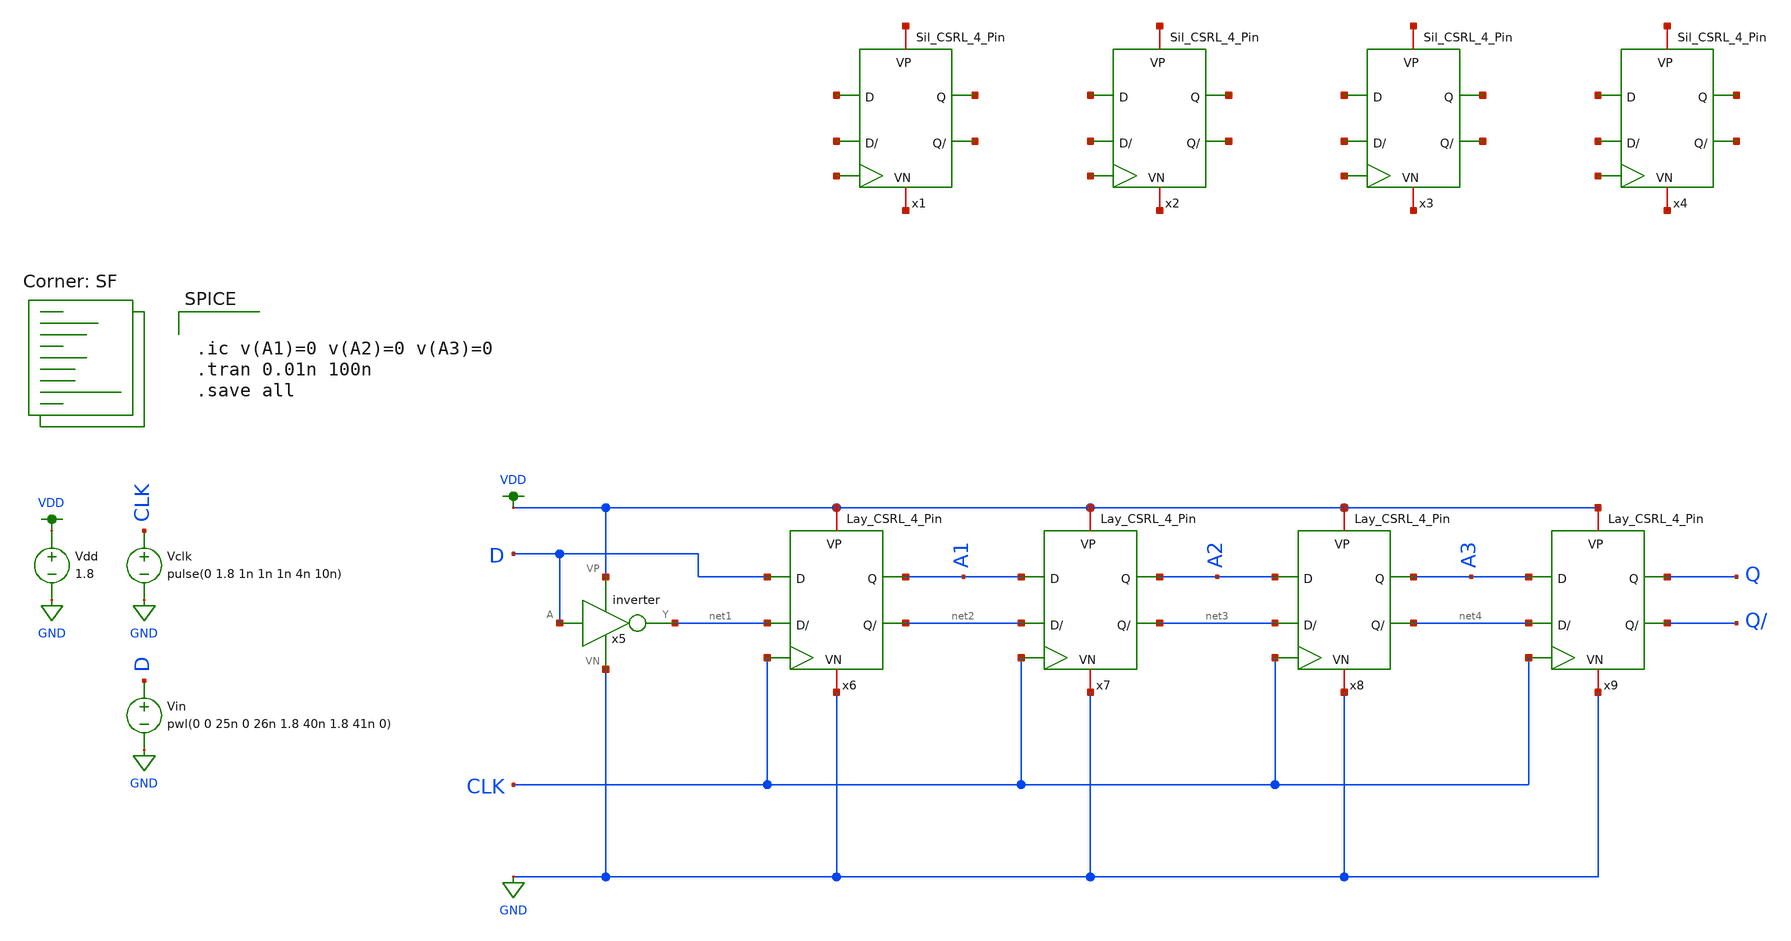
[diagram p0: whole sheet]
** sch_path: MADVLSI_MP2/Shift_Reg_V1.sch
**.subckt Shift_Reg_V1
x5 VDD D net1 GND inverter
Vdd VDD GND 1.8
Vclk CLK GND pulse(0 1.8 1n 1n 1n 4n 10n)
Vin D GND pwl(0 0 25n 0 26n 1.8 40n 1.8 41n 0)
x1 net5 net6 net7 net8 net9 net10 net11 Sil_CSRL_4_Pin
x2 net12 net13 net14 net15 net16 net17 net18 Sil_CSRL_4_Pin
x3 net19 net20 net21 net22 net23 net24 net25 Sil_CSRL_4_Pin
x4 net26 net27 net28 net29 net30 net31 net32 Sil_CSRL_4_Pin
x6 net1 CLK D VDD net2 A1 GND Lay_CSRL_4_Pin
x7 net2 CLK A1 VDD net3 A2 GND Lay_CSRL_4_Pin
x8 net3 CLK A2 VDD net4 A3 GND Lay_CSRL_4_Pin
x9 net4 CLK A3 VDD Q/ Q GND Lay_CSRL_4_Pin
**** begin user architecture code


.ic v(A1)=0 v(A2)=0 v(A3)=0
.tran 0.01n 100n
.save all

.lib $::SKYWATER_MODELS/sky130.lib.spice SF
**** end user architecture code
**.ends

* expanding   symbol:  /home/allan/Documents/MADVLSI_Projects/MADVLSI_MP1/inverter.sym # of pins=4
** sym_path: MADVLSI_MP1/inverter.sym
** sch_path: MADVLSI_MP1/inverter.sch
.subckt inverter VP A Y VN
*.ipin A
*.iopin VP
*.iopin VN
*.opin Y
XM1 Y A VN VN sky130_fd_pr__nfet_01v8 L=0.15 W=1 nf=1 ad='int((nf+1)/2) * W/nf * 0.29' as='int((nf+2)/2) * W/nf * 0.29'
+ pd='2*int((nf+1)/2) * (W/nf + 0.29)' ps='2*int((nf+2)/2) * (W/nf + 0.29)' nrd='0.29 / W' nrs='0.29 / W'
+ sa=0 sb=0 sd=0 mult=1 m=1
XM2 Y A VP VP sky130_fd_pr__pfet_01v8 L=0.15 W=1 nf=1 ad='int((nf+1)/2) * W/nf * 0.29' as='int((nf+2)/2) * W/nf * 0.29'
+ pd='2*int((nf+1)/2) * (W/nf + 0.29)' ps='2*int((nf+2)/2) * (W/nf + 0.29)' nrd='0.29 / W' nrs='0.29 / W'
+ sa=0 sb=0 sd=0 mult=1 m=1
.ends


* expanding   symbol:  Sil_CSRL_4_Pin.sym # of pins=7
** sym_path: MADVLSI_MP2/Sil_CSRL_4_Pin.sym
** sch_path: MADVLSI_MP2/Sil_CSRL_4_Pin.sch
.subckt Sil_CSRL_4_Pin VP D Q QBar DBar clk VN
*.iopin VN
*.iopin VP
*.ipin D
*.ipin DBar
*.ipin clk
*.opin Q
*.opin QBar
XQ1 net1 clk D VP sky130_fd_pr__pfet_01v8 L=0.15 W=0.9 nf=1 ad='int((nf+1)/2) * W/nf * 0.29' as='int((nf+2)/2) * W/nf * 0.29'
+ pd='2*int((nf+1)/2) * (W/nf + 0.29)' ps='2*int((nf+2)/2) * (W/nf + 0.29)' nrd='0.29 / W' nrs='0.29 / W'
+ sa=0 sb=0 sd=0 mult=1 m=1
XQ3 Q clk net1 VN sky130_fd_pr__nfet_01v8 L=0.15 W=0.9 nf=1 ad='int((nf+1)/2) * W/nf * 0.29' as='int((nf+2)/2) * W/nf * 0.29'
+ pd='2*int((nf+1)/2) * (W/nf + 0.29)' ps='2*int((nf+2)/2) * (W/nf + 0.29)' nrd='0.29 / W' nrs='0.29 / W'
+ sa=0 sb=0 sd=0 mult=1 m=1
XQ2 net2 clk DBar VP sky130_fd_pr__pfet_01v8 L=0.15 W=0.9 nf=1 ad='int((nf+1)/2) * W/nf * 0.29' as='int((nf+2)/2) * W/nf * 0.29'
+ pd='2*int((nf+1)/2) * (W/nf + 0.29)' ps='2*int((nf+2)/2) * (W/nf + 0.29)' nrd='0.29 / W' nrs='0.29 / W'
+ sa=0 sb=0 sd=0 mult=1 m=1
XQ8 net2 net1 VP VP sky130_fd_pr__pfet_01v8 L=0.15 W=0.9 nf=1 ad='int((nf+1)/2) * W/nf * 0.29' as='int((nf+2)/2) * W/nf * 0.29'
+ pd='2*int((nf+1)/2) * (W/nf + 0.29)' ps='2*int((nf+2)/2) * (W/nf + 0.29)' nrd='0.29 / W' nrs='0.29 / W'
+ sa=0 sb=0 sd=0 mult=1 m=1
XQ9 VP net2 net1 VP sky130_fd_pr__pfet_01v8 L=0.15 W=0.9 nf=1 ad='int((nf+1)/2) * W/nf * 0.29' as='int((nf+2)/2) * W/nf * 0.29'
+ pd='2*int((nf+1)/2) * (W/nf + 0.29)' ps='2*int((nf+2)/2) * (W/nf + 0.29)' nrd='0.29 / W' nrs='0.29 / W'
+ sa=0 sb=0 sd=0 mult=1 m=1
XQ12 net4 QBar Q VP sky130_fd_pr__pfet_01v8 L=0.15 W=0.9 nf=1 ad='int((nf+1)/2) * W/nf * 0.29' as='int((nf+2)/2) * W/nf * 0.29'
+ pd='2*int((nf+1)/2) * (W/nf + 0.29)' ps='2*int((nf+2)/2) * (W/nf + 0.29)' nrd='0.29 / W' nrs='0.29 / W'
+ sa=0 sb=0 sd=0 mult=1 m=1
XQ10 net4 clk VP VP sky130_fd_pr__pfet_01v8 L=0.15 W=0.9 nf=1 ad='int((nf+1)/2) * W/nf * 0.29' as='int((nf+2)/2) * W/nf * 0.29'
+ pd='2*int((nf+1)/2) * (W/nf + 0.29)' ps='2*int((nf+2)/2) * (W/nf + 0.29)' nrd='0.29 / W' nrs='0.29 / W'
+ sa=0 sb=0 sd=0 mult=1 m=1
XQ11 QBar Q net4 VP sky130_fd_pr__pfet_01v8 L=0.15 W=0.9 nf=1 ad='int((nf+1)/2) * W/nf * 0.29' as='int((nf+2)/2) * W/nf * 0.29'
+ pd='2*int((nf+1)/2) * (W/nf + 0.29)' ps='2*int((nf+2)/2) * (W/nf + 0.29)' nrd='0.29 / W' nrs='0.29 / W'
+ sa=0 sb=0 sd=0 mult=1 m=1
XQ4 QBar clk net2 VN sky130_fd_pr__nfet_01v8 L=0.15 W=0.9 nf=1 ad='int((nf+1)/2) * W/nf * 0.29' as='int((nf+2)/2) * W/nf * 0.29'
+ pd='2*int((nf+1)/2) * (W/nf + 0.29)' ps='2*int((nf+2)/2) * (W/nf + 0.29)' nrd='0.29 / W' nrs='0.29 / W'
+ sa=0 sb=0 sd=0 mult=1 m=1
XQ5a net3 clk VN VN sky130_fd_pr__nfet_01v8 L=0.15 W=0.45 nf=1 ad='int((nf+1)/2) * W/nf * 0.29' as='int((nf+2)/2) * W/nf * 0.29'
+ pd='2*int((nf+1)/2) * (W/nf + 0.29)' ps='2*int((nf+2)/2) * (W/nf + 0.29)' nrd='0.29 / W' nrs='0.29 / W'
+ sa=0 sb=0 sd=0 mult=1 m=1
XQ7 net3 net2 net1 VN sky130_fd_pr__nfet_01v8 L=0.15 W=0.45 nf=1 ad='int((nf+1)/2) * W/nf * 0.29' as='int((nf+2)/2) * W/nf * 0.29'
+ pd='2*int((nf+1)/2) * (W/nf + 0.29)' ps='2*int((nf+2)/2) * (W/nf + 0.29)' nrd='0.29 / W' nrs='0.29 / W'
+ sa=0 sb=0 sd=0 mult=1 m=1
XQ6 net2 net1 net3 VN sky130_fd_pr__nfet_01v8 L=0.15 W=0.45 nf=1 ad='int((nf+1)/2) * W/nf * 0.29' as='int((nf+2)/2) * W/nf * 0.29'
+ pd='2*int((nf+1)/2) * (W/nf + 0.29)' ps='2*int((nf+2)/2) * (W/nf + 0.29)' nrd='0.29 / W' nrs='0.29 / W'
+ sa=0 sb=0 sd=0 mult=1 m=1
XQ13 QBar Q VN VN sky130_fd_pr__nfet_01v8 L=0.15 W=0.45 nf=1 ad='int((nf+1)/2) * W/nf * 0.29' as='int((nf+2)/2) * W/nf * 0.29'
+ pd='2*int((nf+1)/2) * (W/nf + 0.29)' ps='2*int((nf+2)/2) * (W/nf + 0.29)' nrd='0.29 / W' nrs='0.29 / W'
+ sa=0 sb=0 sd=0 mult=1 m=1
XQ14 VN QBar Q VN sky130_fd_pr__nfet_01v8 L=0.15 W=0.45 nf=1 ad='int((nf+1)/2) * W/nf * 0.29' as='int((nf+2)/2) * W/nf * 0.29'
+ pd='2*int((nf+1)/2) * (W/nf + 0.29)' ps='2*int((nf+2)/2) * (W/nf + 0.29)' nrd='0.29 / W' nrs='0.29 / W'
+ sa=0 sb=0 sd=0 mult=1 m=1
XQ5b VN clk net3 VN sky130_fd_pr__nfet_01v8 L=0.15 W=0.45 nf=1 ad='int((nf+1)/2) * W/nf * 0.29' as='int((nf+2)/2) * W/nf * 0.29'
+ pd='2*int((nf+1)/2) * (W/nf + 0.29)' ps='2*int((nf+2)/2) * (W/nf + 0.29)' nrd='0.29 / W' nrs='0.29 / W'
+ sa=0 sb=0 sd=0 mult=1 m=1
XQ10b VP clk net4 VP sky130_fd_pr__pfet_01v8 L=0.15 W=0.9 nf=1 ad='int((nf+1)/2) * W/nf * 0.29' as='int((nf+2)/2) * W/nf * 0.29'
+ pd='2*int((nf+1)/2) * (W/nf + 0.29)' ps='2*int((nf+2)/2) * (W/nf + 0.29)' nrd='0.29 / W' nrs='0.29 / W'
+ sa=0 sb=0 sd=0 mult=1 m=1
.ends


* expanding   symbol:  /home/allan/Documents/MADVLSI_Projects/MADVLSI_MP2/Lay_CSRL_4_Pin.sym # of
*+ pins=7
** sym_path: MADVLSI_MP2/Lay_CSRL_4_Pin.sym
** sch_path: MADVLSI_MP2/Lay_CSRL_4_Pin.sch
.subckt Lay_CSRL_4_Pin D/ CLQ D VP Q/ Q VN
*.ipin D/
*.ipin D
*.ipin CLQ
*.iopin VP
*.iopin VN
*.opin Q/
*.opin Q
XQ2 net3 CLQ D/ VDD sky130_fd_pr__pfet_01v8 L=0.15 W=0.9 nf=1 ad='int((nf+1)/2) * W/nf * 0.29' as='int((nf+2)/2) * W/nf * 0.29'
+ pd='2*int((nf+1)/2) * (W/nf + 0.29)' ps='2*int((nf+2)/2) * (W/nf + 0.29)' nrd='0.29 / W' nrs='0.29 / W'
+ sa=0 sb=0 sd=0 mult=1 m=1
XQ8 VP net1 net3 VDD sky130_fd_pr__pfet_01v8 L=0.15 W=0.9 nf=1 ad='int((nf+1)/2) * W/nf * 0.29' as='int((nf+2)/2) * W/nf * 0.29'
+ pd='2*int((nf+1)/2) * (W/nf + 0.29)' ps='2*int((nf+2)/2) * (W/nf + 0.29)' nrd='0.29 / W' nrs='0.29 / W'
+ sa=0 sb=0 sd=0 mult=1 m=1
XQ10b net2 CLQ VP VDD sky130_fd_pr__pfet_01v8 L=0.15 W=0.9 nf=1 ad='int((nf+1)/2) * W/nf * 0.29' as='int((nf+2)/2) * W/nf * 0.29'
+ pd='2*int((nf+1)/2) * (W/nf + 0.29)' ps='2*int((nf+2)/2) * (W/nf + 0.29)' nrd='0.29 / W' nrs='0.29 / W'
+ sa=0 sb=0 sd=0 mult=1 m=1
XQ11 Q/ Q net2 VDD sky130_fd_pr__pfet_01v8 L=0.15 W=0.9 nf=1 ad='int((nf+1)/2) * W/nf * 0.29' as='int((nf+2)/2) * W/nf * 0.29'
+ pd='2*int((nf+1)/2) * (W/nf + 0.29)' ps='2*int((nf+2)/2) * (W/nf + 0.29)' nrd='0.29 / W' nrs='0.29 / W'
+ sa=0 sb=0 sd=0 mult=1 m=1
XQ1 net1 CLQ D VDD sky130_fd_pr__pfet_01v8 L=0.15 W=0.9 nf=1 ad='int((nf+1)/2) * W/nf * 0.29' as='int((nf+2)/2) * W/nf * 0.29'
+ pd='2*int((nf+1)/2) * (W/nf + 0.29)' ps='2*int((nf+2)/2) * (W/nf + 0.29)' nrd='0.29 / W' nrs='0.29 / W'
+ sa=0 sb=0 sd=0 mult=1 m=1
XQ9 VP net3 net1 VDD sky130_fd_pr__pfet_01v8 L=0.15 W=0.9 nf=1 ad='int((nf+1)/2) * W/nf * 0.29' as='int((nf+2)/2) * W/nf * 0.29'
+ pd='2*int((nf+1)/2) * (W/nf + 0.29)' ps='2*int((nf+2)/2) * (W/nf + 0.29)' nrd='0.29 / W' nrs='0.29 / W'
+ sa=0 sb=0 sd=0 mult=1 m=1
XQ10a net2 CLQ VP VDD sky130_fd_pr__pfet_01v8 L=0.15 W=0.9 nf=1 ad='int((nf+1)/2) * W/nf * 0.29' as='int((nf+2)/2) * W/nf * 0.29'
+ pd='2*int((nf+1)/2) * (W/nf + 0.29)' ps='2*int((nf+2)/2) * (W/nf + 0.29)' nrd='0.29 / W' nrs='0.29 / W'
+ sa=0 sb=0 sd=0 mult=1 m=1
XQ12 Q Q/ net2 VDD sky130_fd_pr__pfet_01v8 L=0.15 W=0.9 nf=1 ad='int((nf+1)/2) * W/nf * 0.29' as='int((nf+2)/2) * W/nf * 0.29'
+ pd='2*int((nf+1)/2) * (W/nf + 0.29)' ps='2*int((nf+2)/2) * (W/nf + 0.29)' nrd='0.29 / W' nrs='0.29 / W'
+ sa=0 sb=0 sd=0 mult=1 m=1
XQ5a net4 CLQ VN GND sky130_fd_pr__nfet_01v8 L=0.15 W=0.45 nf=1 ad='int((nf+1)/2) * W/nf * 0.29' as='int((nf+2)/2) * W/nf * 0.29'
+ pd='2*int((nf+1)/2) * (W/nf + 0.29)' ps='2*int((nf+2)/2) * (W/nf + 0.29)' nrd='0.29 / W' nrs='0.29 / W'
+ sa=0 sb=0 sd=0 mult=1 m=1
XQ6 net3 net1 net4 GND sky130_fd_pr__nfet_01v8 L=0.15 W=0.45 nf=1 ad='int((nf+1)/2) * W/nf * 0.29' as='int((nf+2)/2) * W/nf * 0.29'
+ pd='2*int((nf+1)/2) * (W/nf + 0.29)' ps='2*int((nf+2)/2) * (W/nf + 0.29)' nrd='0.29 / W' nrs='0.29 / W'
+ sa=0 sb=0 sd=0 mult=1 m=1
XQ4 Q/ CLQ net3 GND sky130_fd_pr__nfet_01v8 L=0.15 W=0.9 nf=1 ad='int((nf+1)/2) * W/nf * 0.29' as='int((nf+2)/2) * W/nf * 0.29'
+ pd='2*int((nf+1)/2) * (W/nf + 0.29)' ps='2*int((nf+2)/2) * (W/nf + 0.29)' nrd='0.29 / W' nrs='0.29 / W'
+ sa=0 sb=0 sd=0 mult=1 m=1
XQ13 VN Q Q/ GND sky130_fd_pr__nfet_01v8 L=1.5 W=0.45 nf=1 ad='int((nf+1)/2) * W/nf * 0.29' as='int((nf+2)/2) * W/nf * 0.29'
+ pd='2*int((nf+1)/2) * (W/nf + 0.29)' ps='2*int((nf+2)/2) * (W/nf + 0.29)' nrd='0.29 / W' nrs='0.29 / W'
+ sa=0 sb=0 sd=0 mult=1 m=1
XQ5b net4 CLQ VN GND sky130_fd_pr__nfet_01v8 L=0.15 W=0.45 nf=1 ad='int((nf+1)/2) * W/nf * 0.29' as='int((nf+2)/2) * W/nf * 0.29'
+ pd='2*int((nf+1)/2) * (W/nf + 0.29)' ps='2*int((nf+2)/2) * (W/nf + 0.29)' nrd='0.29 / W' nrs='0.29 / W'
+ sa=0 sb=0 sd=0 mult=1 m=1
XQ7 net1 net3 net4 GND sky130_fd_pr__nfet_01v8 L=0.15 W=0.45 nf=1 ad='int((nf+1)/2) * W/nf * 0.29' as='int((nf+2)/2) * W/nf * 0.29'
+ pd='2*int((nf+1)/2) * (W/nf + 0.29)' ps='2*int((nf+2)/2) * (W/nf + 0.29)' nrd='0.29 / W' nrs='0.29 / W'
+ sa=0 sb=0 sd=0 mult=1 m=1
XQ3 Q CLQ net1 GND sky130_fd_pr__nfet_01v8 L=0.15 W=0.9 nf=1 ad='int((nf+1)/2) * W/nf * 0.29' as='int((nf+2)/2) * W/nf * 0.29'
+ pd='2*int((nf+1)/2) * (W/nf + 0.29)' ps='2*int((nf+2)/2) * (W/nf + 0.29)' nrd='0.29 / W' nrs='0.29 / W'
+ sa=0 sb=0 sd=0 mult=1 m=1
XQ14 VN Q/ Q GND sky130_fd_pr__nfet_01v8 L=0.15 W=0.45 nf=1 ad='int((nf+1)/2) * W/nf * 0.29' as='int((nf+2)/2) * W/nf * 0.29'
+ pd='2*int((nf+1)/2) * (W/nf + 0.29)' ps='2*int((nf+2)/2) * (W/nf + 0.29)' nrd='0.29 / W' nrs='0.29 / W'
+ sa=0 sb=0 sd=0 mult=1 m=1
.ends

.GLOBAL GND
.GLOBAL VDD
.end
